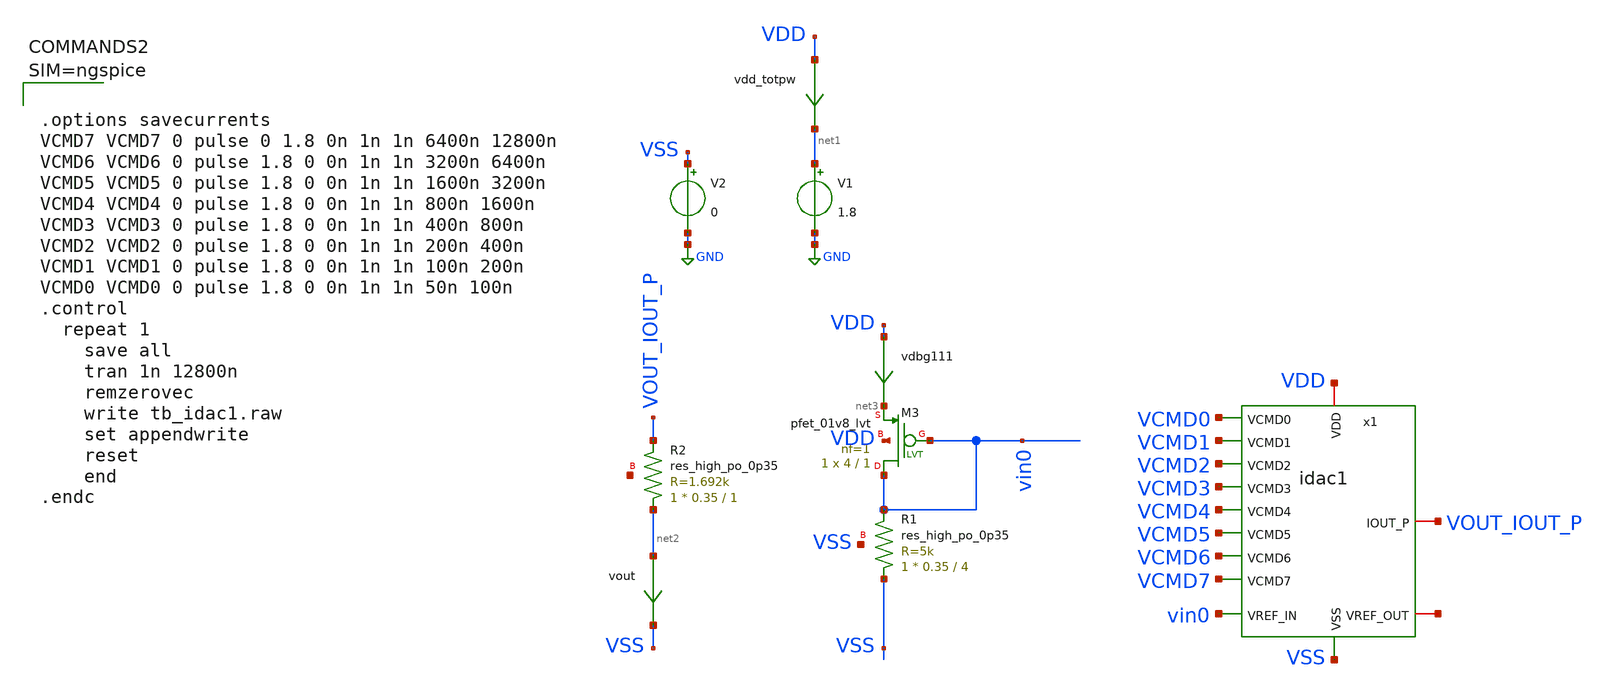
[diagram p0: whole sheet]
** sch_path: tt_um_emilian_rf_playground/xschem/tb_idac1.sch
**.subckt tb_idac1
V1 net1 GND 1.8
V2 VSS GND 0
XM3 vin0 vin0 net3 VDD sky130_fd_pr__pfet_01v8_lvt L=1 W=4 nf=1 ad='int((nf+1)/2) * W/nf * 0.29' as='int((nf+2)/2) * W/nf * 0.29'
+ pd='2*int((nf+1)/2) * (W/nf + 0.29)' ps='2*int((nf+2)/2) * (W/nf + 0.29)' nrd='0.29 / W' nrs='0.29 / W'
+ sa=0 sb=0 sd=0 mult=1 m=1
vout net2 VSS 0
.save i(vout)
XR1 VSS vin0 VSS sky130_fd_pr__res_high_po_0p35 L=4 mult=1 m=1
vdbg111 VDD net3 0
.save i(vdbg111)
XR2 net2 VOUT_IOUT_P net4 sky130_fd_pr__res_high_po_0p35 L=1 mult=1 m=1
vdd_totpw VDD net1 0
.save i(vdd_totpw)
x1 VCMD0 VCMD1 VCMD2 VCMD3 VCMD4 VCMD5 VCMD6 VCMD7 VDD vin0 VSS net5 VOUT_IOUT_P idac1
**** begin user architecture code

** opencircuitdesign pdks install
.lib $::SKYWATER_MODELS/sky130.lib.spice tt_mm
*.lib $::SKYWATER_STDCELLS/sky130_fd_sc_hd_blablabla.spice

.subckt sky130_fd_sc_hd__inv_1 A VGND VNB VPB VPWR Y
X0 VGND A Y VNB sky130_fd_pr__nfet_01v8 w=650000u l=150000u
X1 VPWR A Y VPB sky130_fd_pr__pfet_01v8_hvt w=1e+06u l=150000u
.ends





.options savecurrents
VCMD7 VCMD7 0 pulse 0 1.8 0n 1n 1n 6400n 12800n
VCMD6 VCMD6 0 pulse 1.8 0 0n 1n 1n 3200n 6400n
VCMD5 VCMD5 0 pulse 1.8 0 0n 1n 1n 1600n 3200n
VCMD4 VCMD4 0 pulse 1.8 0 0n 1n 1n 800n 1600n
VCMD3 VCMD3 0 pulse 1.8 0 0n 1n 1n 400n 800n
VCMD2 VCMD2 0 pulse 1.8 0 0n 1n 1n 200n 400n
VCMD1 VCMD1 0 pulse 1.8 0 0n 1n 1n 100n 200n
VCMD0 VCMD0 0 pulse 1.8 0 0n 1n 1n 50n 100n
.control
  repeat 1
    save all
    tran 1n 12800n
    remzerovec
    write tb_idac1.raw
    set appendwrite
    reset
    end
.endc



**** end user architecture code
**.ends

* expanding   symbol:  idac1.sym # of pins=13
** sym_path: tt_um_emilian_rf_playground/xschem/idac1.sym
** sch_path: tt_um_emilian_rf_playground/xschem/idac1.sch
.subckt idac1 VCMD0 VCMD1 VCMD2 VCMD3 VCMD4 VCMD5 VCMD6 VCMD7 VDD VREF_IN VSS VREF_OUT IOUT_P
*.ipin VSS
*.iopin VREF_IN
*.iopin VDD
*.ipin VCMD7
*.ipin VCMD6
*.ipin VCMD5
*.ipin VCMD4
*.ipin VCMD3
*.ipin VCMD2
*.ipin VCMD1
*.ipin VCMD0
*.iopin VREF_OUT
*.iopin IOUT_P
xcell7 vin6 VREF_OUT IOUT VDD VSS VCMD0 idac1cell
xcell6 vin5 vin6 IOUT VDD VSS VCMD1 idac1cell
xcell5 vin4 vin5 IOUT VDD VSS VCMD2 idac1cell
xcell4 vin3 vin4 IOUT VDD VSS VCMD3 idac1cell
xcell3 vin2 vin3 IOUT VDD VSS VCMD4 idac1cell
xcell2 vin1 vin2 IOUT VDD VSS VCMD5 idac1cell
xcell1 vin0 vin1 IOUT VDD VSS VCMD6 idac1cell
xcell0 VREF_IN vin0 IOUT VDD VSS VCMD7 idac1cell
XM2 IOUT IOUT net1 VDD sky130_fd_pr__pfet_01v8_lvt L=1 W=4 nf=1 ad='int((nf+1)/2) * W/nf * 0.29' as='int((nf+2)/2) * W/nf * 0.29'
+ pd='2*int((nf+1)/2) * (W/nf + 0.29)' ps='2*int((nf+2)/2) * (W/nf + 0.29)' nrd='0.29 / W' nrs='0.29 / W'
+ sa=0 sb=0 sd=0 mult=1 m=1
vdbg1 VDD net1 0
.save i(vdbg1)
XM4 IOUT_P IOUT net2 VDD sky130_fd_pr__pfet_01v8_lvt L=1 W=4 nf=1 ad='int((nf+1)/2) * W/nf * 0.29' as='int((nf+2)/2) * W/nf * 0.29'
+ pd='2*int((nf+1)/2) * (W/nf + 0.29)' ps='2*int((nf+2)/2) * (W/nf + 0.29)' nrd='0.29 / W' nrs='0.29 / W'
+ sa=0 sb=0 sd=0 mult=1 m=1
vdbg2 VDD net2 0
.save i(vdbg2)
.ends


* expanding   symbol:  idac1cell.sym # of pins=6
** sym_path: tt_um_emilian_rf_playground/xschem/idac1cell.sym
** sch_path: tt_um_emilian_rf_playground/xschem/idac1cell.sch
.subckt idac1cell VREF_IN VREF_OUT IOUT VDD VSS OE
*.ipin VSS
*.iopin VREF_OUT
*.ipin VREF_IN
*.iopin VDD
*.iopin IOUT
*.ipin OE
XM3 net1 net1 net2 net2 sky130_fd_pr__nfet_01v8_lvt L=1 W=2 nf=1 ad='int((nf+1)/2) * W/nf * 0.29' as='int((nf+2)/2) * W/nf * 0.29'
+ pd='2*int((nf+1)/2) * (W/nf + 0.29)' ps='2*int((nf+2)/2) * (W/nf + 0.29)' nrd='0.29 / W' nrs='0.29 / W'
+ sa=0 sb=0 sd=0 mult=1 m=1
XM4 net1 net1 VSS VSS sky130_fd_pr__nfet_01v8_lvt L=1 W=2 nf=1 ad='int((nf+1)/2) * W/nf * 0.29' as='int((nf+2)/2) * W/nf * 0.29'
+ pd='2*int((nf+1)/2) * (W/nf + 0.29)' ps='2*int((nf+2)/2) * (W/nf + 0.29)' nrd='0.29 / W' nrs='0.29 / W'
+ sa=0 sb=0 sd=0 mult=1 m=1
XM1 net1 VREF_IN VDD VDD sky130_fd_pr__pfet_01v8_lvt L=1 W=4 nf=1 ad='int((nf+1)/2) * W/nf * 0.29' as='int((nf+2)/2) * W/nf * 0.29'
+ pd='2*int((nf+1)/2) * (W/nf + 0.29)' ps='2*int((nf+2)/2) * (W/nf + 0.29)' nrd='0.29 / W' nrs='0.29 / W'
+ sa=0 sb=0 sd=0 mult=1 m=1
XM5 net3 net1 VSS VSS sky130_fd_pr__nfet_01v8_lvt L=1 W=2 nf=1 ad='int((nf+1)/2) * W/nf * 0.29' as='int((nf+2)/2) * W/nf * 0.29'
+ pd='2*int((nf+1)/2) * (W/nf + 0.29)' ps='2*int((nf+2)/2) * (W/nf + 0.29)' nrd='0.29 / W' nrs='0.29 / W'
+ sa=0 sb=0 sd=0 mult=1 m=1
XM2 VREF_OUT VREF_OUT VDD VDD sky130_fd_pr__pfet_01v8_lvt L=1 W=4 nf=1 ad='int((nf+1)/2) * W/nf * 0.29'
+ as='int((nf+2)/2) * W/nf * 0.29' pd='2*int((nf+1)/2) * (W/nf + 0.29)' ps='2*int((nf+2)/2) * (W/nf + 0.29)'
+ nrd='0.29 / W' nrs='0.29 / W' sa=0 sb=0 sd=0 mult=1 m=1
XM6 vdrain2 net1 VSS VSS sky130_fd_pr__nfet_01v8_lvt L=1 W=2 nf=1 ad='int((nf+1)/2) * W/nf * 0.29' as='int((nf+2)/2) * W/nf * 0.29'
+ pd='2*int((nf+1)/2) * (W/nf + 0.29)' ps='2*int((nf+2)/2) * (W/nf + 0.29)' nrd='0.29 / W' nrs='0.29 / W'
+ sa=0 sb=0 sd=0 mult=1 m=1
XM7 net4 OE vdrain2 VSS sky130_fd_pr__nfet_01v8_lvt L=1 W=2 nf=1 ad='int((nf+1)/2) * W/nf * 0.29' as='int((nf+2)/2) * W/nf * 0.29'
+ pd='2*int((nf+1)/2) * (W/nf + 0.29)' ps='2*int((nf+2)/2) * (W/nf + 0.29)' nrd='0.29 / W' nrs='0.29 / W'
+ sa=0 sb=0 sd=0 mult=1 m=1
vmeas VREF_OUT net3 0
.save i(vmeas)
viout IOUT net4 0
.save i(viout)
vref net2 VSS 0
.save i(vref)
.ends

.GLOBAL GND
.end
